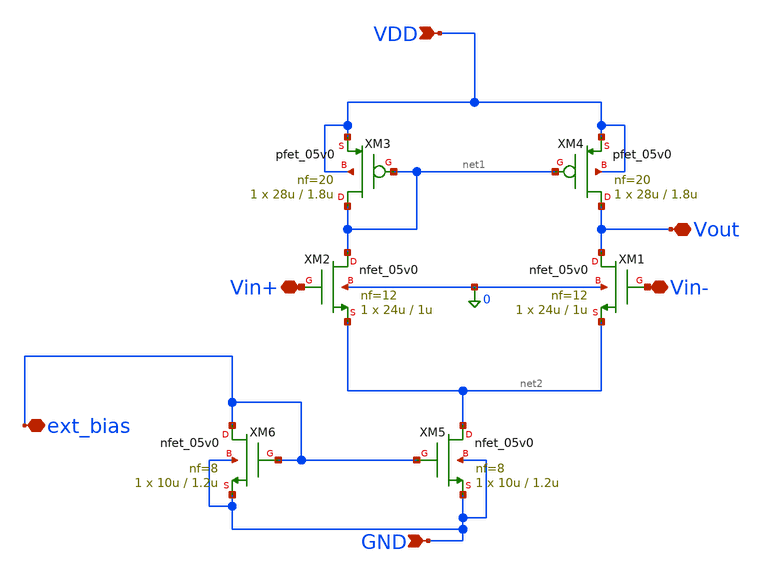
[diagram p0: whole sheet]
** sch_path: TG_gm_ff_testing/gm_ff.sch
**.subckt gm_ff GND VDD ext_bias Vin- Vin+ Vout
*.ipin GND
*.ipin VDD
*.iopin ext_bias
*.iopin Vin-
*.iopin Vin+
*.iopin Vout
XM1 Vout Vin- net2 0 nfet_05v0 L=1u W=24u nf=12 ad='int((nf+1)/2) * W/nf * 0.18u' as='int((nf+2)/2) * W/nf * 0.18u'
+ pd='2*int((nf+1)/2) * (W/nf + 0.18u)' ps='2*int((nf+2)/2) * (W/nf + 0.18u)' nrd='0.18u / W' nrs='0.18u / W'
+ sa=0 sb=0 sd=0 m=1
XM2 net1 Vin+ net2 0 nfet_05v0 L=1u W=24u nf=12 ad='int((nf+1)/2) * W/nf * 0.18u' as='int((nf+2)/2) * W/nf * 0.18u'
+ pd='2*int((nf+1)/2) * (W/nf + 0.18u)' ps='2*int((nf+2)/2) * (W/nf + 0.18u)' nrd='0.18u / W' nrs='0.18u / W'
+ sa=0 sb=0 sd=0 m=1
XM5 net2 ext_bias GND GND nfet_05v0 L=1.2u W=10u nf=8 ad='int((nf+1)/2) * W/nf * 0.18u' as='int((nf+2)/2) * W/nf * 0.18u'
+ pd='2*int((nf+1)/2) * (W/nf + 0.18u)' ps='2*int((nf+2)/2) * (W/nf + 0.18u)' nrd='0.18u / W' nrs='0.18u / W'
+ sa=0 sb=0 sd=0 m=1
XM4 Vout net1 VDD VDD pfet_05v0 L=1.8u W=28u nf=20 ad='int((nf+1)/2) * W/nf * 0.18u' as='int((nf+2)/2) * W/nf * 0.18u'
+ pd='2*int((nf+1)/2) * (W/nf + 0.18u)' ps='2*int((nf+2)/2) * (W/nf + 0.18u)' nrd='0.18u / W' nrs='0.18u / W'
+ sa=0 sb=0 sd=0 m=1
XM3 net1 net1 VDD VDD pfet_05v0 L=1.8u W=28u nf=20 ad='int((nf+1)/2) * W/nf * 0.18u' as='int((nf+2)/2) * W/nf * 0.18u'
+ pd='2*int((nf+1)/2) * (W/nf + 0.18u)' ps='2*int((nf+2)/2) * (W/nf + 0.18u)' nrd='0.18u / W' nrs='0.18u / W'
+ sa=0 sb=0 sd=0 m=1
XM6 ext_bias ext_bias GND GND nfet_05v0 L=1.2u W=10u nf=8 ad='int((nf+1)/2) * W/nf * 0.18u' as='int((nf+2)/2) * W/nf * 0.18u'
+ pd='2*int((nf+1)/2) * (W/nf + 0.18u)' ps='2*int((nf+2)/2) * (W/nf + 0.18u)' nrd='0.18u / W' nrs='0.18u / W'
+ sa=0 sb=0 sd=0 m=1
**.ends
.end
